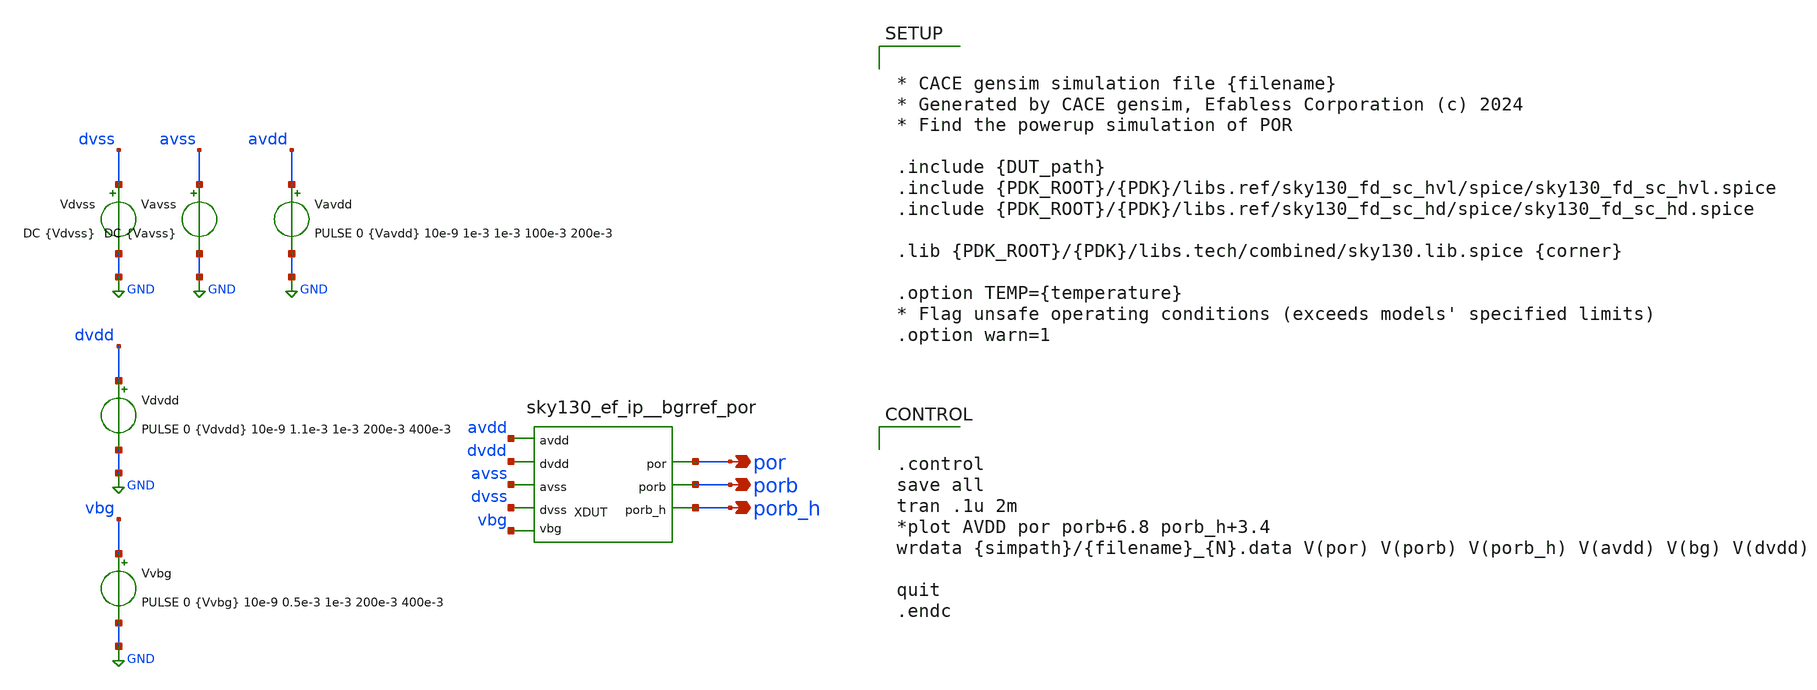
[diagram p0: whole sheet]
** sch_path: cace/startup_sim.sch
**.subckt startup_sim por porb porb_h
*.opin por
*.opin porb
*.opin porb_h
XDUT vbg por avss avdd dvdd porb dvss porb_h VCC VSS sky130_ef_ip__bgrref_por W_N=1 L_N=0.2 W_P=1
+ L_P=0.2 m=1
Vdvss dvss GND DC {Vdvss}
Vavdd avdd GND PULSE 0 {Vavdd} 10e-9 1e-3 1e-3 100e-3 200e-3
Vavss avss GND DC {Vavss}
Vdvdd dvdd GND PULSE 0 {Vdvdd} 10e-9 1.1e-3 1e-3 200e-3 400e-3
Vvbg vbg GND PULSE 0 {Vvbg} 10e-9 0.5e-3 1e-3 200e-3 400e-3
**** begin user architecture code


* CACE gensim simulation file {filename}
* Generated by CACE gensim, Efabless Corporation (c) 2024
* Find the powerup simulation of POR

.include {DUT_path}
.include {PDK_ROOT}/{PDK}/libs.ref/sky130_fd_sc_hvl/spice/sky130_fd_sc_hvl.spice
.include {PDK_ROOT}/{PDK}/libs.ref/sky130_fd_sc_hd/spice/sky130_fd_sc_hd.spice

.lib {PDK_ROOT}/{PDK}/libs.tech/combined/sky130.lib.spice {corner}

.option TEMP={temperature}
* Flag unsafe operating conditions (exceeds models' specified limits)
.option warn=1




.control
save all
tran .1u 2m
*plot AVDD por porb+6.8 porb_h+3.4
wrdata {simpath}/{filename}_{N}.data V(por) V(porb) V(porb_h) V(avdd) V(bg) V(dvdd)

quit
.endc


**** end user architecture code
**.ends
.GLOBAL GND
.end
